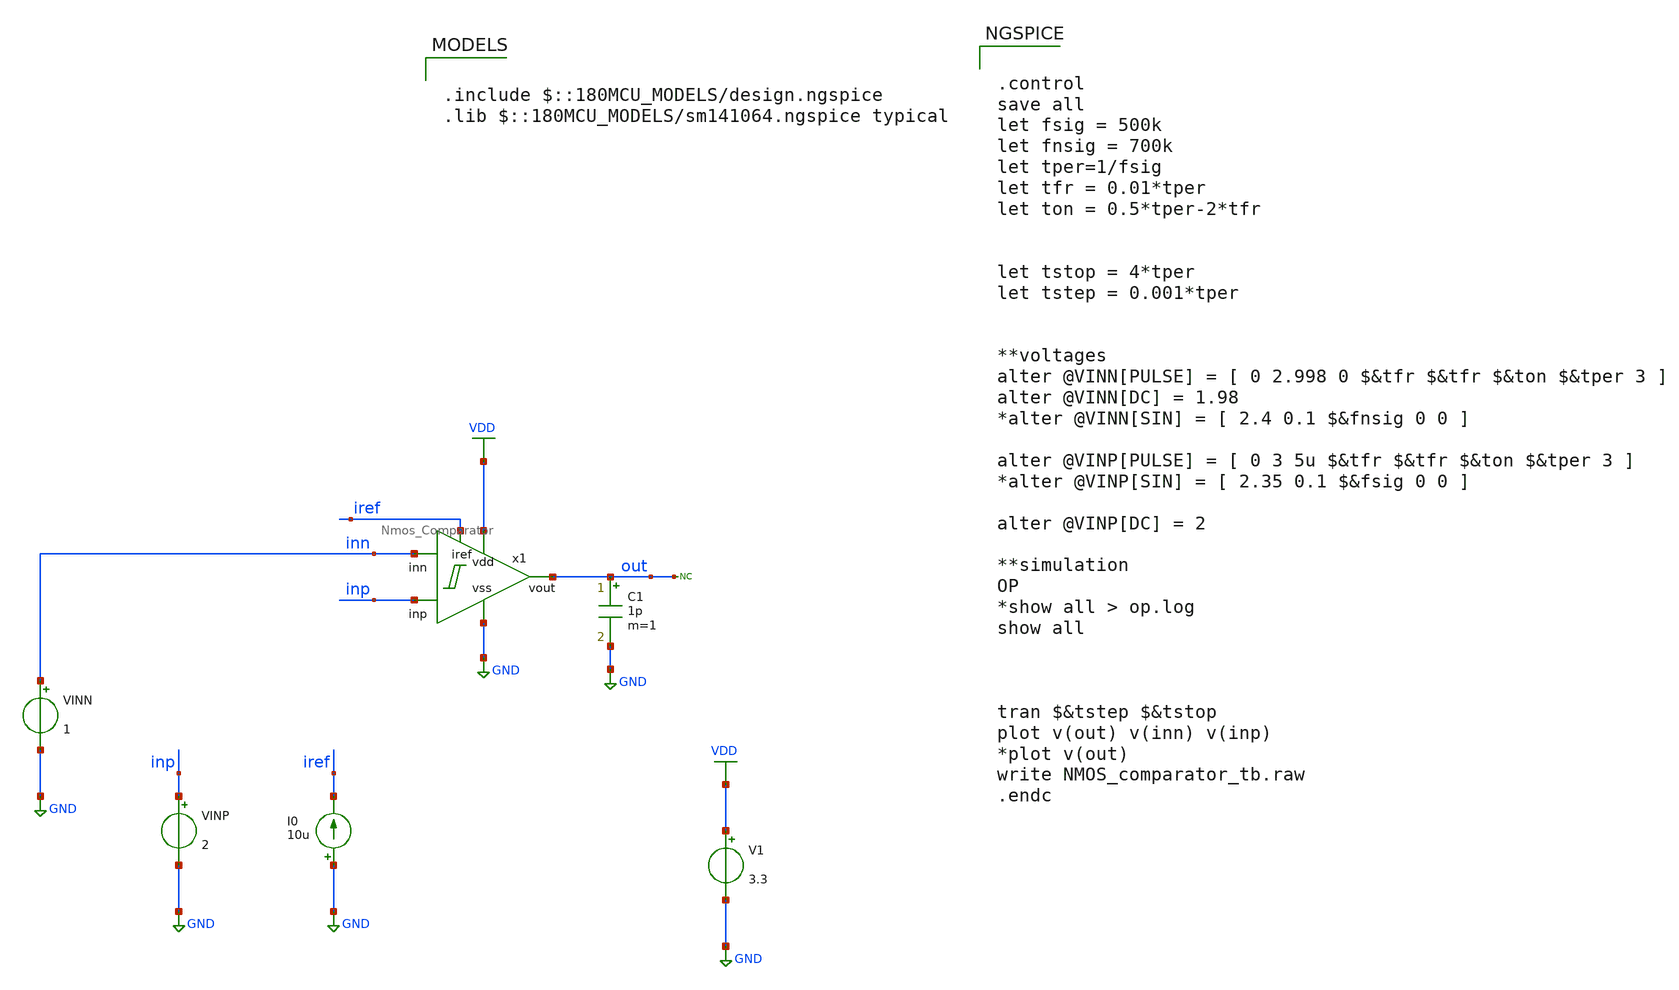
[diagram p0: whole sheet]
** sch_path: designs/libs/tb_analog/Comparator/NMOS_comparator_tb.sch
**.subckt NMOS_comparator_tb
I0 GND iref 10u
V1 VDD GND 3.3
VINP inp GND 2
* noconn out
VINN inn GND 1
x1 VDD out inp GND inn iref Nmos_Comparator
C1 out GND 1p m=1
**** begin user architecture code


.control
save all
let fsig = 500k
let fnsig = 700k
let tper=1/fsig
let tfr = 0.01*tper
let ton = 0.5*tper-2*tfr


let tstop = 4*tper
let tstep = 0.001*tper


**voltages
alter @VINN[PULSE] = [ 0 2.998 0 $&tfr $&tfr $&ton $&tper 3 ]
alter @VINN[DC] = 1.98
*alter @VINN[SIN] = [ 2.4 0.1 $&fnsig 0 0 ]

alter @VINP[PULSE] = [ 0 3 5u $&tfr $&tfr $&ton $&tper 3 ]
*alter @VINP[SIN] = [ 2.35 0.1 $&fsig 0 0 ]

alter @VINP[DC] = 2

**simulation
OP
*show all > op.log
show all



tran $&tstep $&tstop
plot v(out) v(inn) v(inp)
*plot v(out)
write NMOS_comparator_tb.raw
.endc



.include $::180MCU_MODELS/design.ngspice
.lib $::180MCU_MODELS/sm141064.ngspice typical

**** end user architecture code
**.ends

* expanding   symbol:  libs/core_analog/Comparator/Nmos_Comparator.sym # of pins=6
** sym_path: designs/libs/core_analog/Comparator/Nmos_Comparator.sym
** sch_path: designs/libs/core_analog/Comparator/Nmos_Comparator.sch
.subckt Nmos_Comparator vdd vout inp vss inn iref
*.ipin vss
*.ipin vdd
*.ipin iref
*.ipin inn
*.ipin inp
*.opin vout
XM3 net1 net1 vss vss nfet_03v3 L=1u W=3.56u nf=1 ad='int((nf+1)/2) * W/nf * 0.18u' as='int((nf+2)/2) * W/nf * 0.18u'
+ pd='2*int((nf+1)/2) * (W/nf + 0.18u)' ps='2*int((nf+2)/2) * (W/nf + 0.18u)' nrd='0.18u / W' nrs='0.18u / W'
+ sa=0 sb=0 sd=0 m=1
XM4 vout net1 vss vss nfet_03v3 L=1u W=3.56u nf=1 ad='int((nf+1)/2) * W/nf * 0.18u' as='int((nf+2)/2) * W/nf * 0.18u'
+ pd='2*int((nf+1)/2) * (W/nf + 0.18u)' ps='2*int((nf+2)/2) * (W/nf + 0.18u)' nrd='0.18u / W' nrs='0.18u / W'
+ sa=0 sb=0 sd=0 m=1
XM5 net2 inn net3 vss nfet_03v3 L=1u W=4.13u nf=1 ad='int((nf+1)/2) * W/nf * 0.18u' as='int((nf+2)/2) * W/nf * 0.18u'
+ pd='2*int((nf+1)/2) * (W/nf + 0.18u)' ps='2*int((nf+2)/2) * (W/nf + 0.18u)' nrd='0.18u / W' nrs='0.18u / W'
+ sa=0 sb=0 sd=0 m=1
XM6 net4 inp net3 vss nfet_03v3 L=1u W=4.13u nf=1 ad='int((nf+1)/2) * W/nf * 0.18u' as='int((nf+2)/2) * W/nf * 0.18u'
+ pd='2*int((nf+1)/2) * (W/nf + 0.18u)' ps='2*int((nf+2)/2) * (W/nf + 0.18u)' nrd='0.18u / W' nrs='0.18u / W'
+ sa=0 sb=0 sd=0 m=1
XM7 net1 net2 vdd vdd pfet_03v3 L=0.5u W=4.1u nf=4 ad='int((nf+1)/2) * W/nf * 0.18u' as='int((nf+2)/2) * W/nf * 0.18u'
+ pd='2*int((nf+1)/2) * (W/nf + 0.18u)' ps='2*int((nf+2)/2) * (W/nf + 0.18u)' nrd='0.18u / W' nrs='0.18u / W'
+ sa=0 sb=0 sd=0 m=4
XM9 net4 net4 vdd vdd pfet_03v3 L=0.5u W=5u nf=2 ad='int((nf+1)/2) * W/nf * 0.18u' as='int((nf+2)/2) * W/nf * 0.18u'
+ pd='2*int((nf+1)/2) * (W/nf + 0.18u)' ps='2*int((nf+2)/2) * (W/nf + 0.18u)' nrd='0.18u / W' nrs='0.18u / W'
+ sa=0 sb=0 sd=0 m=2
XM11 net2 net2 vdd vdd pfet_03v3 L=0.5u W=5u nf=2 ad='int((nf+1)/2) * W/nf * 0.18u' as='int((nf+2)/2) * W/nf * 0.18u'
+ pd='2*int((nf+1)/2) * (W/nf + 0.18u)' ps='2*int((nf+2)/2) * (W/nf + 0.18u)' nrd='0.18u / W' nrs='0.18u / W'
+ sa=0 sb=0 sd=0 m=2
XM12 vout net4 vdd vdd pfet_03v3 L=0.5u W=4.1u nf=4 ad='int((nf+1)/2) * W/nf * 0.18u' as='int((nf+2)/2) * W/nf * 0.18u'
+ pd='2*int((nf+1)/2) * (W/nf + 0.18u)' ps='2*int((nf+2)/2) * (W/nf + 0.18u)' nrd='0.18u / W' nrs='0.18u / W'
+ sa=0 sb=0 sd=0 m=4
x1 iref vss iref vss unit_nmos M=1
x2 net3 vss iref vss unit_nmos M=2
XM1 net4 net2 vdd vdd pfet_03v3 L=0.5u W=5u nf=2 ad='int((nf+1)/2) * W/nf * 0.18u' as='int((nf+2)/2) * W/nf * 0.18u'
+ pd='2*int((nf+1)/2) * (W/nf + 0.18u)' ps='2*int((nf+2)/2) * (W/nf + 0.18u)' nrd='0.18u / W' nrs='0.18u / W'
+ sa=0 sb=0 sd=0 m=2
XM2 net2 net4 vdd vdd pfet_03v3 L=0.5u W=5u nf=2 ad='int((nf+1)/2) * W/nf * 0.18u' as='int((nf+2)/2) * W/nf * 0.18u'
+ pd='2*int((nf+1)/2) * (W/nf + 0.18u)' ps='2*int((nf+2)/2) * (W/nf + 0.18u)' nrd='0.18u / W' nrs='0.18u / W'
+ sa=0 sb=0 sd=0 m=2
.ends


* expanding   symbol:  libs/core_analog/unit_nmos/unit_nmos.sym # of pins=4
** sym_path: libs/core_analog/unit_nmos/unit_nmos.sym
** sch_path: libs/core_analog/unit_nmos/unit_nmos.sch
.subckt unit_nmos drain sub gate source
*.iopin drain
*.iopin source
*.iopin sub
*.iopin gate
XM1 drain gate source sub nfet_03v3 L=1u W=2.5u nf=1 ad='int((nf+1)/2) * W/nf * 0.18u' as='int((nf+2)/2) * W/nf * 0.18u'
+ pd='2*int((nf+1)/2) * (W/nf + 0.18u)' ps='2*int((nf+2)/2) * (W/nf + 0.18u)' nrd='0.18u / W' nrs='0.18u / W'
+ sa=0 sb=0 sd=0 m={M}
**** begin user architecture code

.param M=1

**** end user architecture code
.ends

.GLOBAL GND
.GLOBAL VDD
.end
